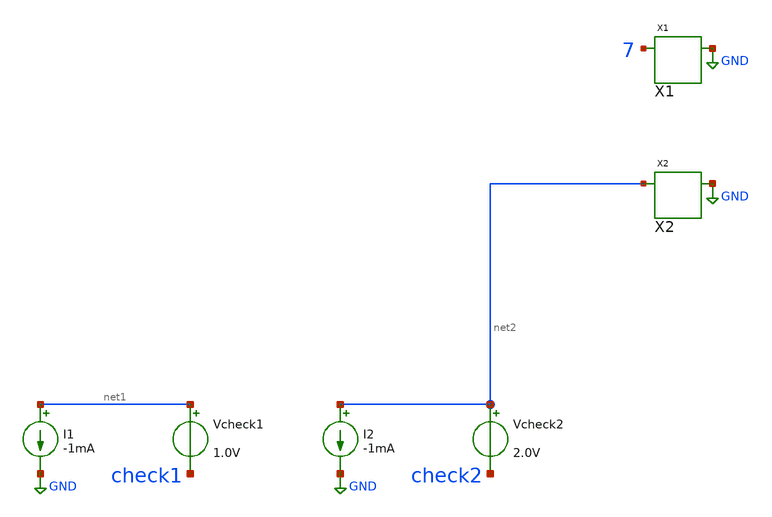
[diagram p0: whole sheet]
** sch_path: data/sch/aicas_ex3a.sch
**.subckt aicas_ex3a
I1 net1 GND -1mA
X1 7 GND sub1_in_lib
Vcheck1 net1 check1 1.0V
I2 net2 GND -1mA
X2 net2 GND sub2_in_lib
Vcheck2 net2 check2 2.0V
**.ends
.GLOBAL GND
.end
